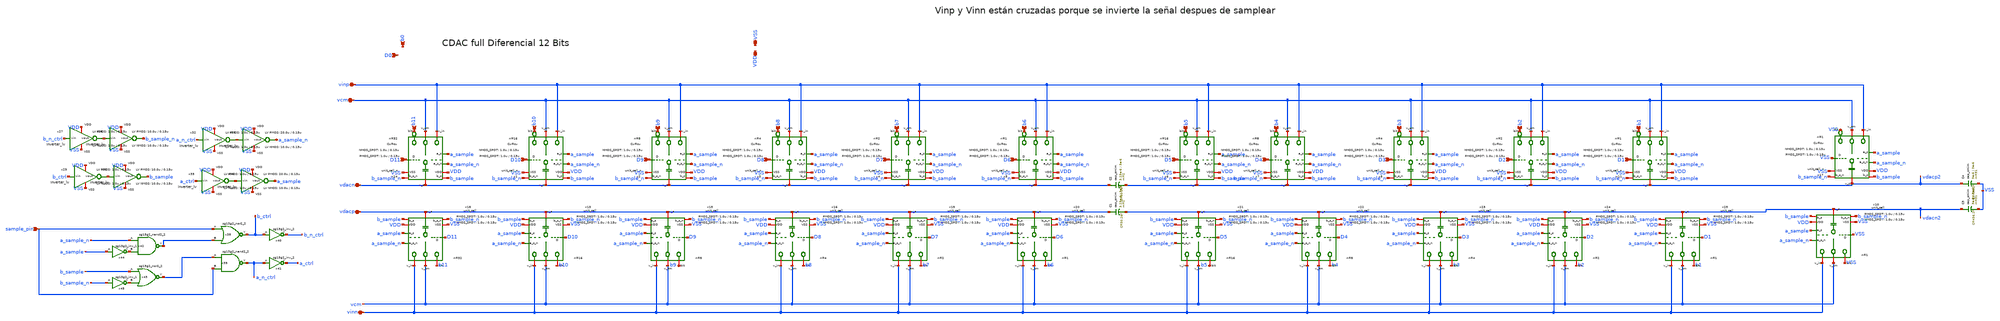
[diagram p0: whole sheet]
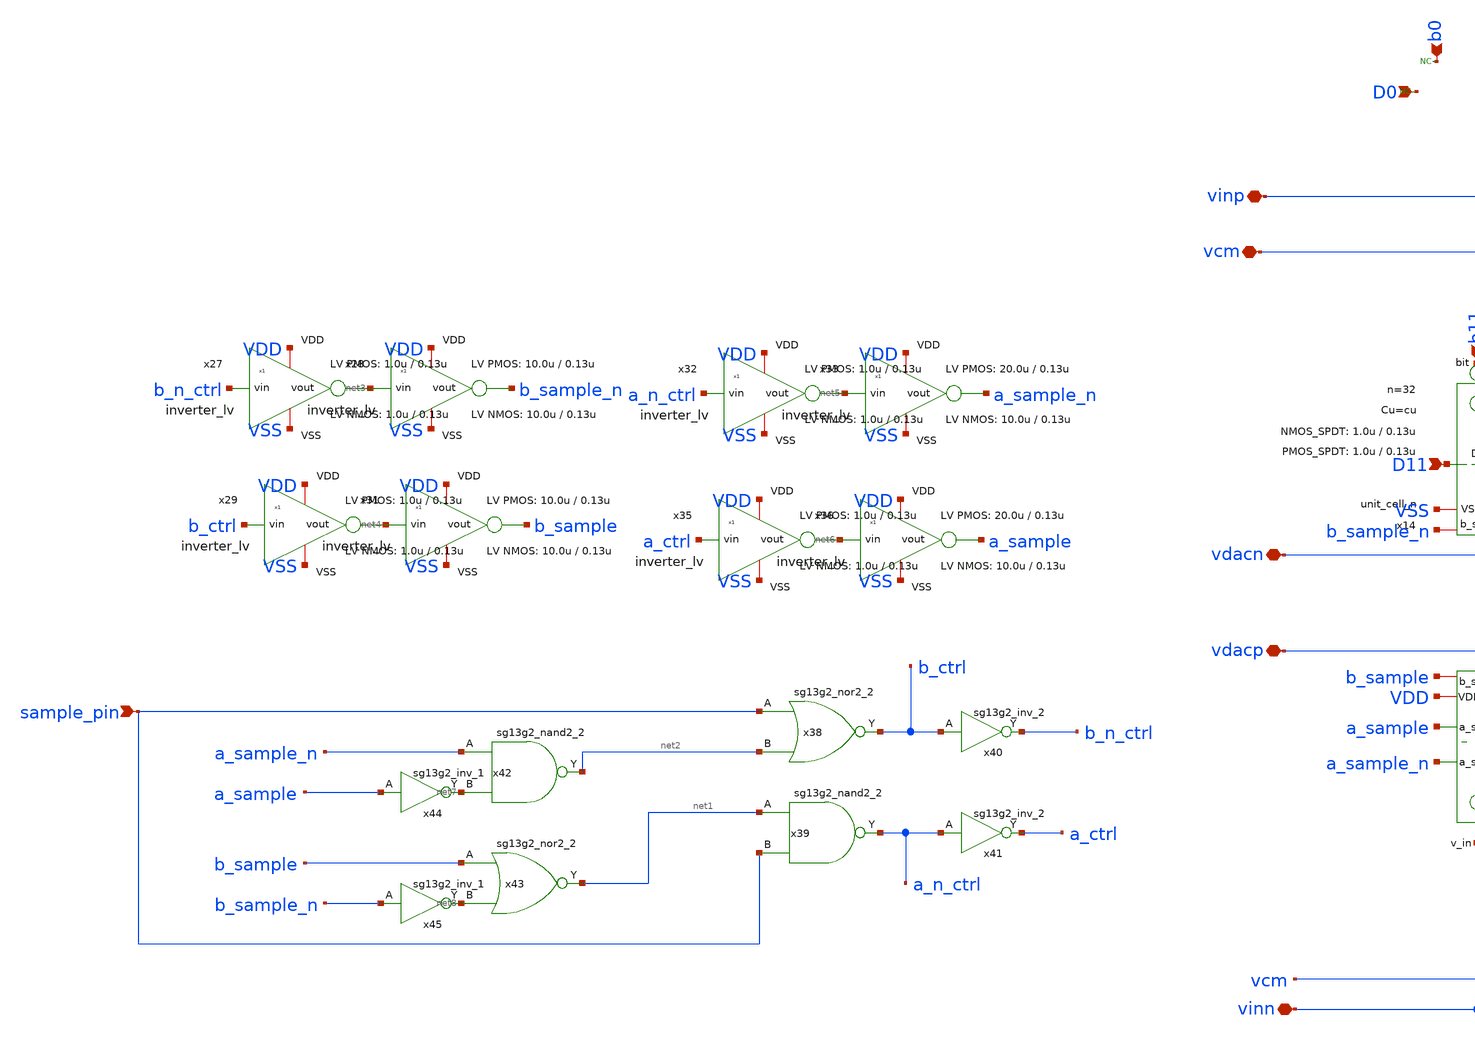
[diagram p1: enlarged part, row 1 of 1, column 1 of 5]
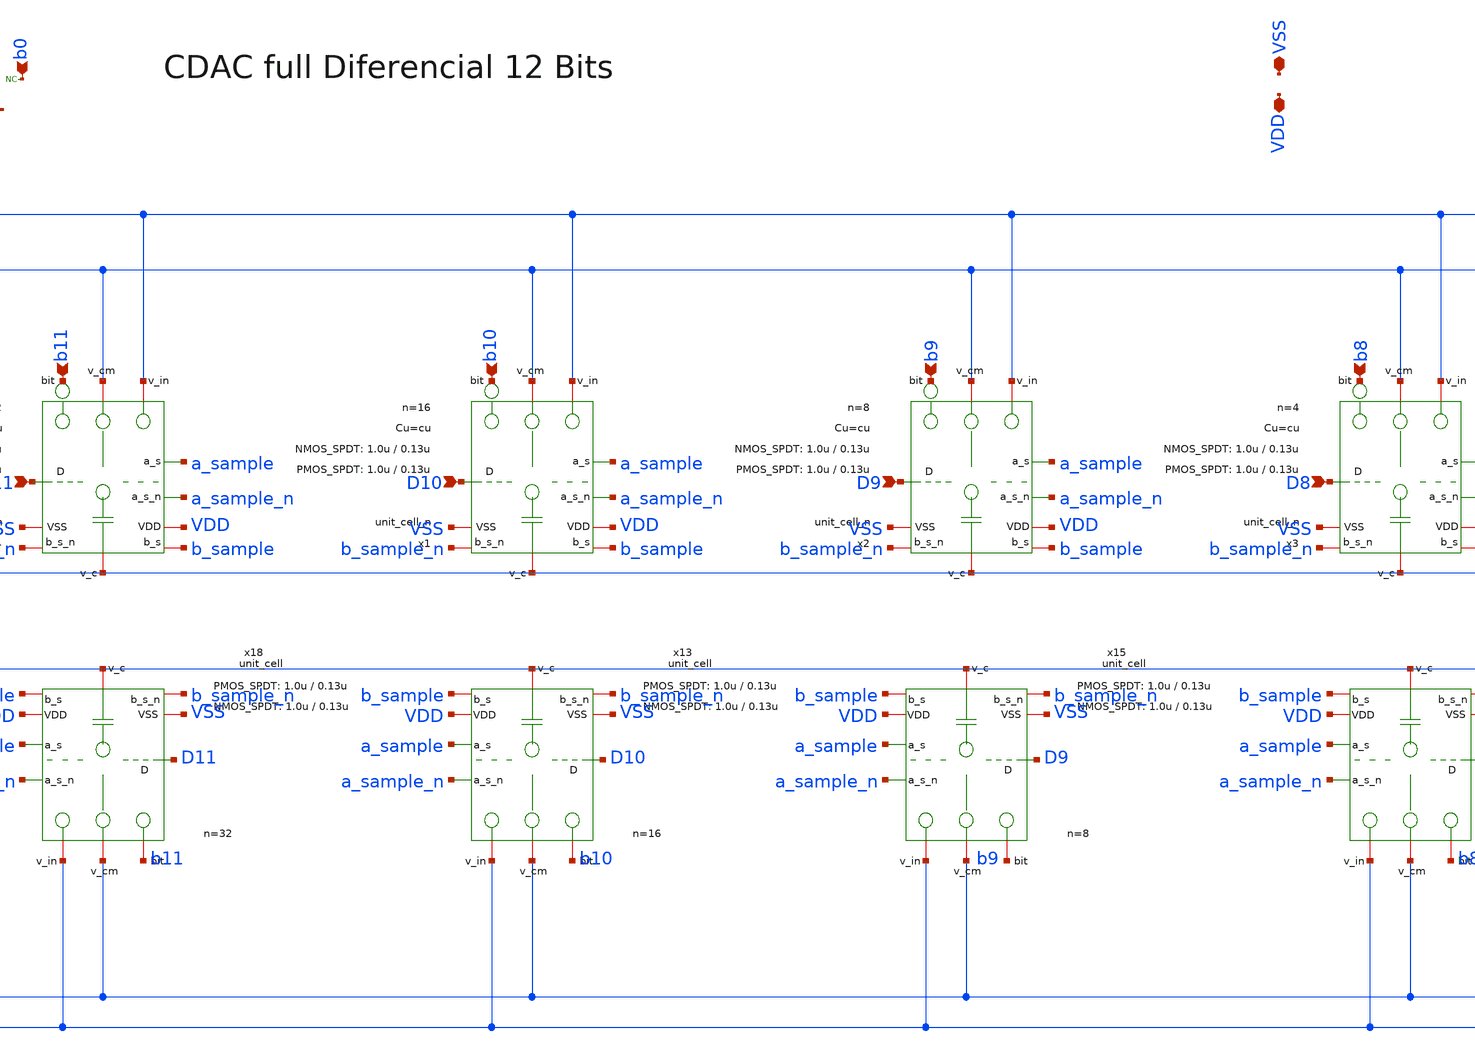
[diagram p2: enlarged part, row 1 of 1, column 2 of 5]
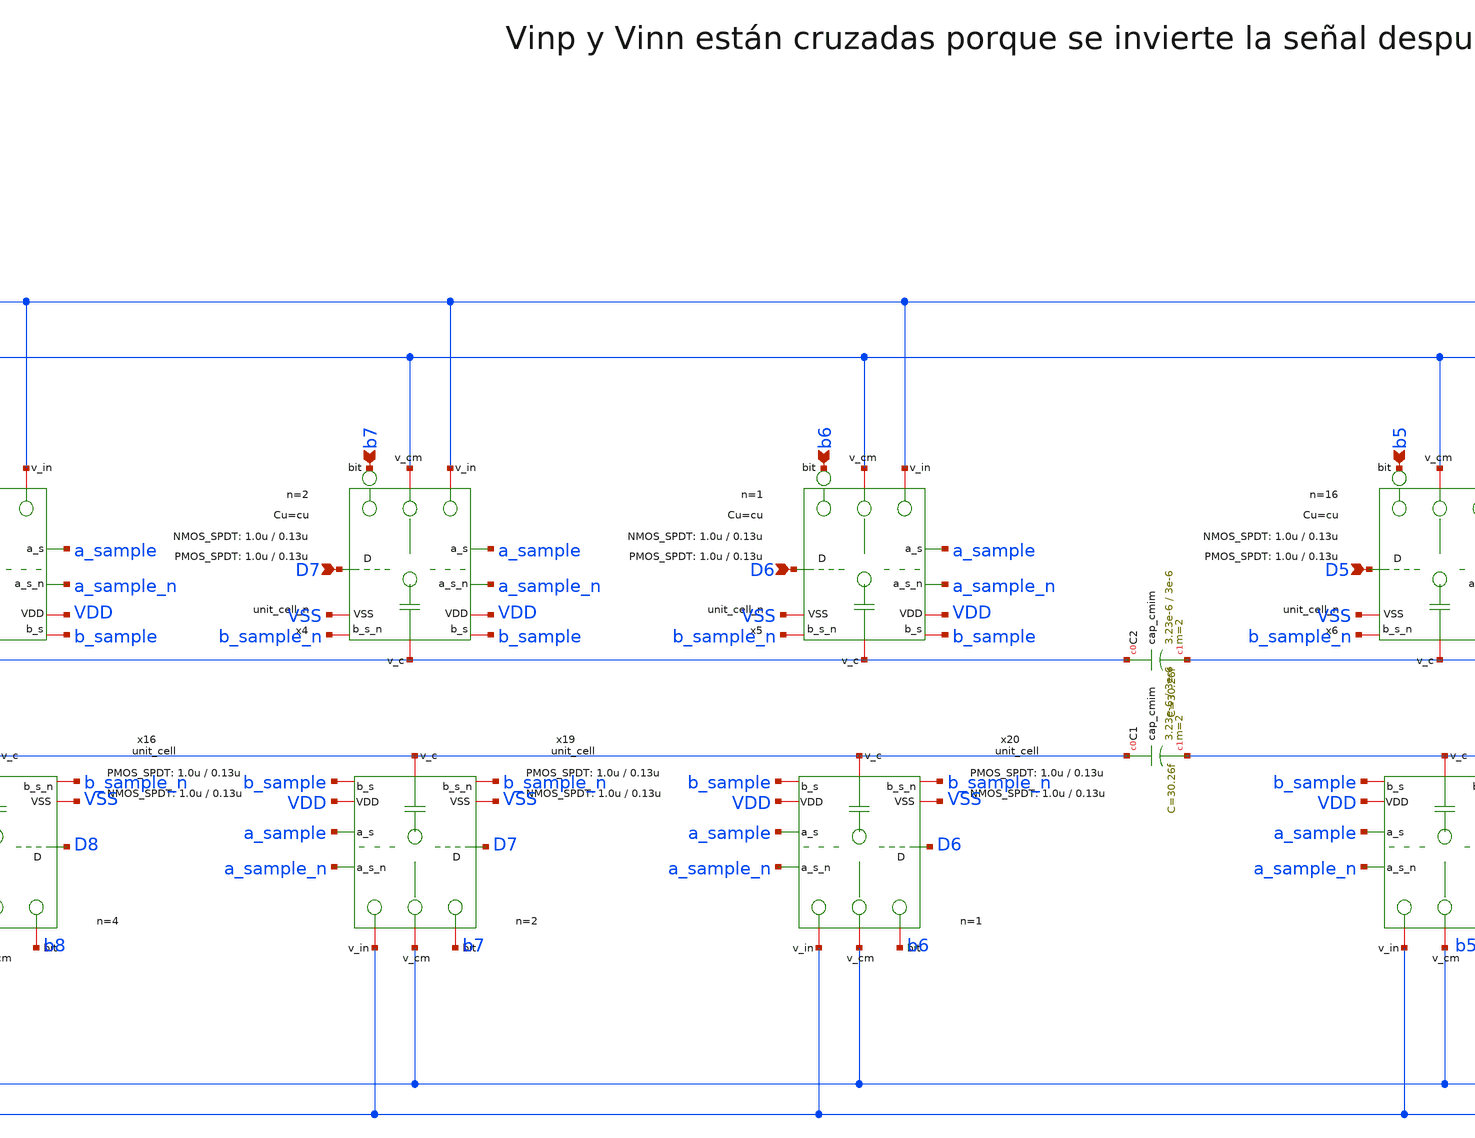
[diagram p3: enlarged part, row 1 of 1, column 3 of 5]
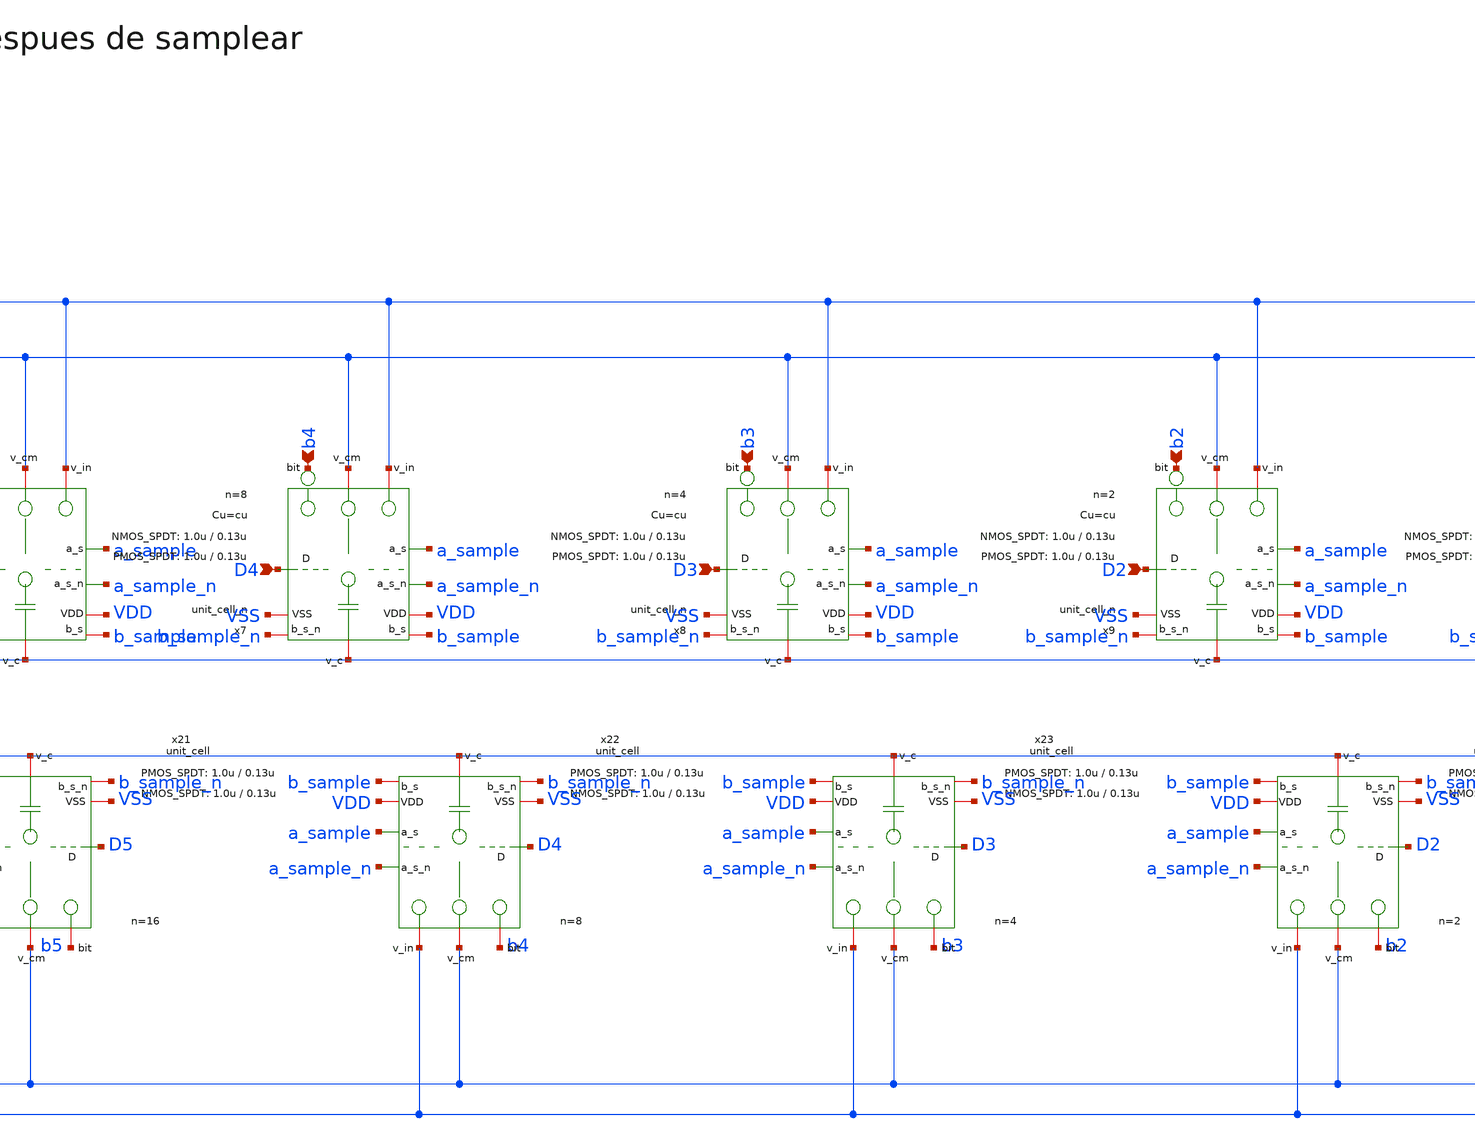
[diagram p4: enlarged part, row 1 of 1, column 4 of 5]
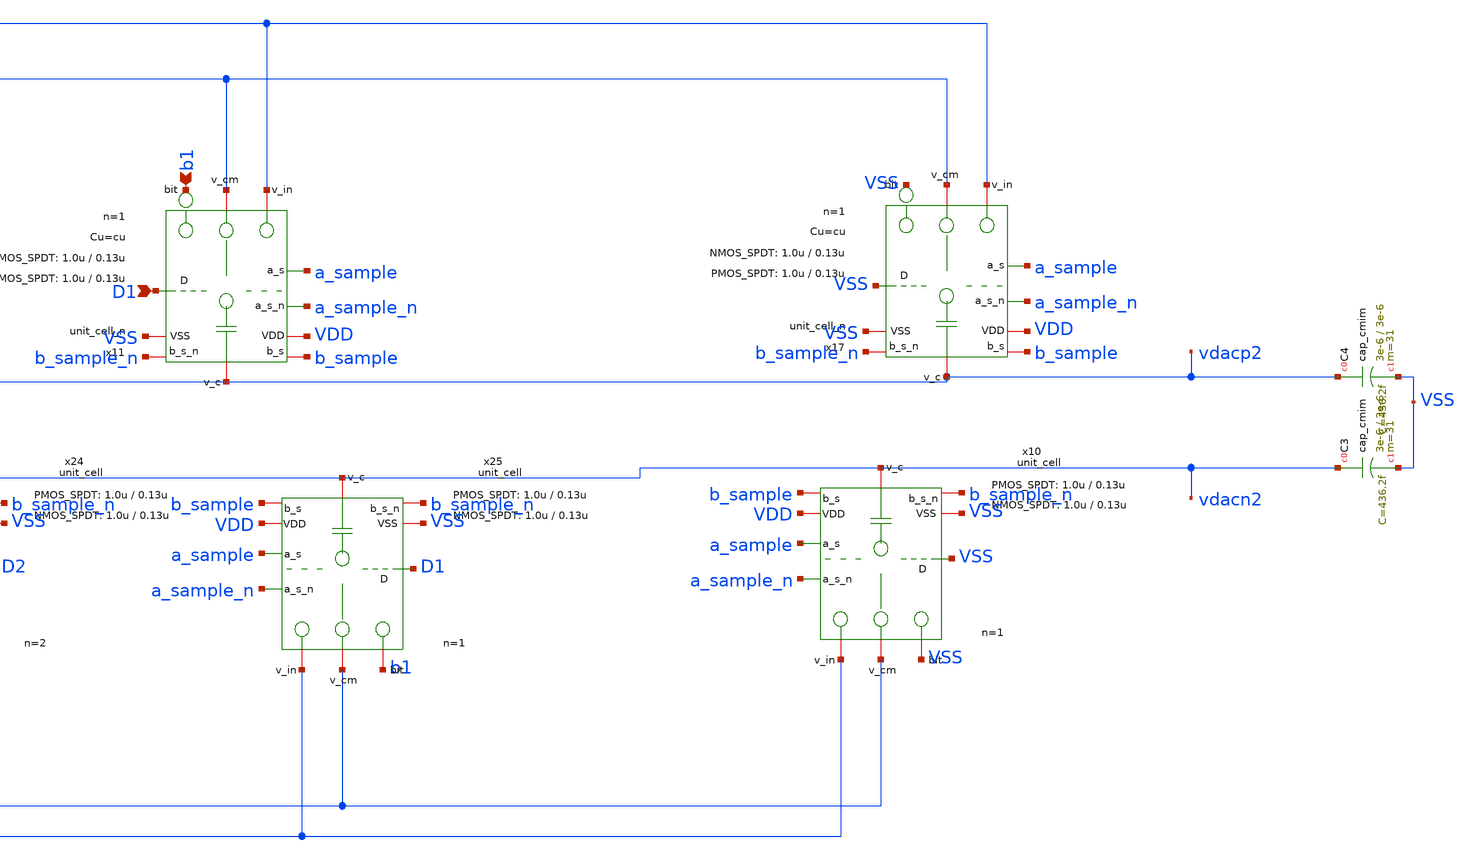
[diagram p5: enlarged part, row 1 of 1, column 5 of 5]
** sch_path: xschem/dac_icms_cell/dac.sch
* IHP-GmbH/IHP-Open-PDK/ihp-sg13g2/libs.tech/xschem/sg13g2_stdcells/sg13g2_inv_2.sch:
* Copyright 2023 IHP PDK Authors
* Licensed under the Apache License, Version 2.0 (the "License");
**.subckt dac D0 b0 vinn vcm sample_pin vinp vdacp vdacn VSS VDD D1 b1 D2 b2 D3 b3 D4 b4 D5 b5 b6 D7
*+ b7 D8 b8 D9 b9 D10 b10 D11 b11 D6
*.ipin D0
*.ipin b0
*.iopin vinn
*.iopin vcm
*.ipin sample_pin
*.iopin vinp
*.iopin vdacp
*.iopin vdacn
*.iopin VSS
*.iopin VDD
*.ipin D1
*.ipin b1
*.ipin D2
*.ipin b2
*.ipin D3
*.ipin b3
*.ipin D4
*.ipin b4
*.ipin D5
*.ipin b5
*.ipin b6
*.ipin D7
*.ipin b7
*.ipin D8
*.ipin b8
*.ipin D9
*.ipin b9
*.ipin D10
*.ipin b10
*.ipin D11
*.ipin b11
*.ipin D6
x14 VDD D11 VSS vdacn b11 vcm vinp a_sample a_sample_n b_sample b_sample_n unit_cell_n W_P=
+ L_P_SPDT=0.13u W_N= L_N_SPDT=0.13u Cu=cu n=32
x18 VDD D11 VSS vdacp b11 vcm vinn a_sample a_sample_n b_sample b_sample_n unit_cell W_P_SPDT=1.0u
+ L_P_SPDT=0.13u W_N_SPDT=1.0u L_N_SPDT=0.13u Cu=cu n=32
x1 VDD D10 VSS vdacn b10 vcm vinp a_sample a_sample_n b_sample b_sample_n unit_cell_n W_P=
+ L_P_SPDT=0.13u W_N= L_N_SPDT=0.13u Cu=cu n=16
x2 VDD D9 VSS vdacn b9 vcm vinp a_sample a_sample_n b_sample b_sample_n unit_cell_n W_P=
+ L_P_SPDT=0.13u W_N= L_N_SPDT=0.13u Cu=cu n=8
x3 VDD D8 VSS vdacn b8 vcm vinp a_sample a_sample_n b_sample b_sample_n unit_cell_n W_P=
+ L_P_SPDT=0.13u W_N= L_N_SPDT=0.13u Cu=cu n=4
x4 VDD D7 VSS vdacn b7 vcm vinp a_sample a_sample_n b_sample b_sample_n unit_cell_n W_P=1.0u
+ L_P_SPDT=0.13u W_N=1.0u L_N_SPDT=0.13u Cu=cu n=2
x5 VDD D6 VSS vdacn b6 vcm vinp a_sample a_sample_n b_sample b_sample_n unit_cell_n W_P=
+ L_P_SPDT=0.13u W_N= L_N_SPDT=0.13u Cu=cu n=1
x6 VDD D5 VSS vdacp2 b5 vcm vinp a_sample a_sample_n b_sample b_sample_n unit_cell_n W_P=
+ L_P_SPDT=0.13u W_N= L_N_SPDT=0.13u Cu=cu n=16
x7 VDD D4 VSS vdacp2 b4 vcm vinp a_sample a_sample_n b_sample b_sample_n unit_cell_n W_P=
+ L_P_SPDT=0.13u W_N= L_N_SPDT=0.13u Cu=cu n=8
x8 VDD D3 VSS vdacp2 b3 vcm vinp a_sample a_sample_n b_sample b_sample_n unit_cell_n W_P=
+ L_P_SPDT=0.13u W_N= L_N_SPDT=0.13u Cu=cu n=4
x9 VDD D2 VSS vdacp2 b2 vcm vinp a_sample a_sample_n b_sample b_sample_n unit_cell_n W_P=
+ L_P_SPDT=0.13u W_N= L_N_SPDT=0.13u Cu=cu n=2
x11 VDD D1 VSS vdacp2 b1 vcm vinp a_sample a_sample_n b_sample b_sample_n unit_cell_n W_P=
+ L_P_SPDT=0.13u W_N= L_N_SPDT=0.13u Cu=cu n=1
x13 VDD D10 VSS vdacp b10 vcm vinn a_sample a_sample_n b_sample b_sample_n unit_cell W_P_SPDT=1.0u
+ L_P_SPDT=0.13u W_N_SPDT=1.0u L_N_SPDT=0.13u Cu=cu n=16
x15 VDD D9 VSS vdacp b9 vcm vinn a_sample a_sample_n b_sample b_sample_n unit_cell W_P_SPDT=1.0u
+ L_P_SPDT=0.13u W_N_SPDT=1.0u L_N_SPDT=0.13u Cu=cu n=8
x16 VDD D8 VSS vdacp b8 vcm vinn a_sample a_sample_n b_sample b_sample_n unit_cell W_P_SPDT=1.0u
+ L_P_SPDT=0.13u W_N_SPDT=1.0u L_N_SPDT=0.13u Cu=cu n=4
x19 VDD D7 VSS vdacp b7 vcm vinn a_sample a_sample_n b_sample b_sample_n unit_cell W_P_SPDT=1.0u
+ L_P_SPDT=0.13u W_N_SPDT=1.0u L_N_SPDT=0.13u Cu=cu n=2
x20 VDD D6 VSS vdacp b6 vcm vinn a_sample a_sample_n b_sample b_sample_n unit_cell W_P_SPDT=1.0u
+ L_P_SPDT=0.13u W_N_SPDT=1.0u L_N_SPDT=0.13u Cu=cu n=1
x21 VDD D5 VSS vdacn2 b5 vcm vinn a_sample a_sample_n b_sample b_sample_n unit_cell W_P_SPDT=1.0u
+ L_P_SPDT=0.13u W_N_SPDT=1.0u L_N_SPDT=0.13u Cu=cu n=16
x22 VDD D4 VSS vdacn2 b4 vcm vinn a_sample a_sample_n b_sample b_sample_n unit_cell W_P_SPDT=1.0u
+ L_P_SPDT=0.13u W_N_SPDT=1.0u L_N_SPDT=0.13u Cu=cu n=8
x23 VDD D3 VSS vdacn2 b3 vcm vinn a_sample a_sample_n b_sample b_sample_n unit_cell W_P_SPDT=1.0u
+ L_P_SPDT=0.13u W_N_SPDT=1.0u L_N_SPDT=0.13u Cu=cu n=4
x24 VDD D2 VSS vdacn2 b2 vcm vinn a_sample a_sample_n b_sample b_sample_n unit_cell W_P_SPDT=1.0u
+ L_P_SPDT=0.13u W_N_SPDT=1.0u L_N_SPDT=0.13u Cu=cu n=2
x25 VDD D1 VSS vdacn2 b1 vcm vinn a_sample a_sample_n b_sample b_sample_n unit_cell W_P_SPDT=1.0u
+ L_P_SPDT=0.13u W_N_SPDT=1.0u L_N_SPDT=0.13u Cu=cu n=1
x27 VDD b_n_ctrl net3 VSS inverter_lv W_P=1.0u L_P=0.13u W_N=1.0u L_N=0.13u N_C=1
x28 VDD net3 b_sample_n VSS inverter_lv W_P=10.0u L_P=0.13u W_N=10.0u L_N=0.13u N_C=1
x29 VDD b_ctrl net4 VSS inverter_lv W_P=1.0u L_P=0.13u W_N=1.0u L_N=0.13u N_C=1
x31 VDD net4 b_sample VSS inverter_lv W_P=10.0u L_P=0.13u W_N=10.0u L_N=0.13u N_C=1
x32 VDD a_n_ctrl net5 VSS inverter_lv W_P=1.0u L_P=0.13u W_N=1.0u L_N=0.13u N_C=1
x33 VDD net5 a_sample_n VSS inverter_lv W_P=20.0u L_P=0.13u W_N=10.0u L_N=0.13u N_C=1
x35 VDD a_ctrl net6 VSS inverter_lv W_P=1.0u L_P=0.13u W_N=1.0u L_N=0.13u N_C=1
x36 VDD net6 a_sample VSS inverter_lv W_P=20.0u L_P=0.13u W_N=10.0u L_N=0.13u N_C=1
x38 b_ctrl sample_pin net2 VDD VSS sg13g2_nor2_2
x39 a_n_ctrl net1 sample_pin VDD VSS sg13g2_nand2_2
x40 b_n_ctrl b_ctrl VDD VSS sg13g2_inv_2
x41 a_ctrl a_n_ctrl VDD VSS sg13g2_inv_2
x42 net2 a_sample_n net7 VDD VSS sg13g2_nand2_2
x43 net1 b_sample net8 VDD VSS sg13g2_nor2_2
x44 net7 a_sample VDD VSS sg13g2_inv_1
x45 net8 b_sample_n VDD VSS sg13g2_inv_1
XC1 vdacp vdacn2 cap_cmim w=3.23e-6 l=3e-6 m=2 mm_ok=1
XC2 vdacn vdacp2 cap_cmim w=3.23e-6 l=3e-6 m=2 mm_ok=1
x10 VDD VSS VSS vdacn2 VSS vcm vinn a_sample a_sample_n b_sample b_sample_n unit_cell W_P_SPDT=1.0u
+ L_P_SPDT=0.13u W_N_SPDT=1.0u L_N_SPDT=0.13u Cu=cu n=1
x17 VDD VSS VSS vdacp2 VSS vcm vinp a_sample a_sample_n b_sample b_sample_n unit_cell_n W_P=
+ L_P_SPDT=0.13u W_N= L_N_SPDT=0.13u Cu=cu n=1
XC3 vdacn2 VSS cap_cmim w=3e-6 l=3e-6 m=31 mm_ok=1
XC4 vdacp2 VSS cap_cmim w=3e-6 l=3e-6 m=31 mm_ok=1
* noconn b0
* noconn D0
**.ends

* expanding   symbol:  dac_icms_cell/unit_cell_n.sym # of pins=11
** sym_path: xschem/dac_icms_cell/unit_cell_n.sym
** sch_path: xschem/dac_icms_cell/unit_cell_n.sch
.subckt unit_cell_n VDD d VSS v_top bit v_cm v_in a_sample a_sample_n b_sample b_sample_n
+  W_P_SPDT=1.0u L_P_SPDT=0.13u W_N_SPDT=1.0u L_N_SPDT=0.13u Cu=8f n=1
*.iopin VSS
*.iopin v_in
*.iopin VDD
*.ipin d
*.ipin bit
*.iopin v_top
*.iopin v_cm
*.ipin a_sample
*.ipin a_sample_n
*.ipin b_sample
*.ipin b_sample_n
x1 VDD d VSS net1 bit v_cm v_in b_sample_n b_sample dac_switch_n W_P_TG=3.0u L_P_TG=0.13u
+ W_N_TG=1.0u L_N_TG=0.13u n=n
C1 net1 v_top Cu m=n
x2 VDD a_sample VSS v_cm v_top a_sample_n transmission_gate_lv_w_dummy W_P=W_P_SPDT L_P=L_P_SPDT
+ W_N=W_N_SPDT L_N=L_N_SPDT W_P_D=1.0u L_P_D=0.13u W_N_D=1.0u L_N_D=0.13u n=n
.ends


* expanding   symbol:  dac_icms_cell/unit_cell.sym # of pins=11
** sym_path: xschem/dac_icms_cell/unit_cell.sym
** sch_path: xschem/dac_icms_cell/unit_cell.sch
.subckt unit_cell VDD d VSS v_top bit v_cm v_in a_sample a_sample_n b_sample b_sample_n
+  W_P_SPDT=1.0u L_P_SPDT=0.13u W_N_SPDT=1.0u L_N_SPDT=0.13u Cu=8f n=1
*.iopin VSS
*.iopin v_in
*.ipin d
*.ipin bit
*.iopin v_top
*.iopin v_cm
*.ipin b_sample
*.ipin b_sample_n
*.ipin a_sample
*.ipin a_sample_n
*.iopin VDD
S7 net2 net3 d VSS SW1
C1 net1 v_top Cu m=n
S9 net3 net1 b_sample b_sample_n SW1
S10 v_in net1 b_sample_n b_sample SW1
S11 v_top v_cm a_sample a_sample_n SW1
S12 VSS net2 bit VSS SW1
S13 net2 VDD bitn VSS SW1
S14 net3 v_cm dn VSS SW1
x8 VDD bit bitn VSS inverter_lv W_P=W_P_SPDT L_P=L_P_SPDT W_N=W_N_SPDT L_N=L_N_SPDT N_C=1
x1 VDD d dn VSS inverter_lv W_P=W_P_SPDT L_P=L_P_SPDT W_N=W_N_SPDT L_N=L_N_SPDT N_C=1
.ends


* expanding   symbol:  inverter/inverter_lv.sym # of pins=4
** sym_path: xschem/inverter/inverter_lv.sym
** sch_path: xschem/inverter/inverter_lv.sch
.subckt inverter_lv VDD vin vout VSS  W_P=3.0u L_P=0.13u W_N=1.0u L_N=0.13u N_C=1
*.ipin vin
*.iopin VDD
*.iopin VSS
*.opin vout
XM1 vout vin VDD VDD sg13_lv_pmos w=W_P l=L_P ng=1 m={N_C} mm_ok=1
XM2 vout vin VSS VSS sg13_lv_nmos w=W_N l=L_N ng=1 m={N_C} mm_ok=1
.ends


* expanding   symbol:  sg13g2_stdcells/sg13g2_nor2_2.sym # of pins=3
** sym_path: sg13g2_stdcells/sg13g2_nor2_2.sym
** sch_path: sg13g2_stdcells/sg13g2_nor2_2.sch
.subckt sg13g2_nor2_2 Y A B VDD VSS
*.opin Y
*.ipin B
*.ipin A
*.iopin VDD
*.iopin VSS
XM1 Y A VSS VSS sg13_lv_nmos w=1.48u l=130.00n ng=2 m=1 mm_ok=1
XM2 Y B VSS VSS sg13_lv_nmos w=1.48u l=130.00n ng=2 m=1 mm_ok=1
XM3 net1 A VDD VDD sg13_lv_pmos w=2.24u l=130.00n ng=2 m=1 mm_ok=1
XM4 Y B net1 VDD sg13_lv_pmos w=2.24u l=130.00n ng=2 m=1 mm_ok=1
.ends


* expanding   symbol:  sg13g2_stdcells/sg13g2_nand2_2.sym # of pins=3
** sym_path: sg13g2_stdcells/sg13g2_nand2_2.sym
** sch_path: sg13g2_stdcells/sg13g2_nand2_2.sch
.subckt sg13g2_nand2_2 Y A B VDD VSS
*.iopin VDD
*.iopin VSS
*.opin Y
*.ipin B
*.ipin A
XM1 Y A net1 VSS sg13_lv_nmos w=1.44u l=130.00n ng=2 m=1 mm_ok=1
XM2 net1 B VSS VSS sg13_lv_nmos w=1.44u l=130.00n ng=2 m=1 mm_ok=1
XM3 Y A VDD VDD sg13_lv_pmos w=2.24u l=130.00n ng=2 m=1 mm_ok=1
XM4 Y B VDD VDD sg13_lv_pmos w=2.24u l=130.00n ng=2 m=1 mm_ok=1
.ends


* expanding   symbol:  sg13g2_stdcells/sg13g2_inv_2.sym # of pins=2
** sym_path: sg13g2_stdcells/sg13g2_inv_2.sym
** sch_path: sg13g2_stdcells/sg13g2_inv_2.sch
.subckt sg13g2_inv_2 Y A VDD VSS
*.opin Y
*.ipin A
*.iopin VDD
*.iopin VSS
XM1 Y A VSS VSS sg13_lv_nmos w=1.48u l=130.00n ng=2 m=1 mm_ok=1
XM2 Y A VDD VDD sg13_lv_pmos w=2.24u l=130.00n ng=2 m=1 mm_ok=1
.ends


* expanding   symbol:  sg13g2_stdcells/sg13g2_inv_1.sym # of pins=2
** sym_path: sg13g2_stdcells/sg13g2_inv_1.sym
** sch_path: sg13g2_stdcells/sg13g2_inv_1.sch
.subckt sg13g2_inv_1 Y A VDD VSS
*.opin Y
*.ipin A
*.iopin VDD
*.iopin VSS
XM1 Y A VSS VSS sg13_lv_nmos w=740.00n l=130.00n ng=1 m=1 mm_ok=1
XM2 Y A VDD VDD sg13_lv_pmos w=1.12u l=130.00n ng=1 m=1 mm_ok=1
.ends


* expanding   symbol:  dac_icms_cell/dac_switch_n.sym # of pins=9
** sym_path: xschem/dac_icms_cell/dac_switch_n.sym
** sch_path: xschem/dac_icms_cell/dac_switch_n.sch
.subckt dac_switch_n VDD d VSS v_cap bit v_cm v_in sample sample_n  W_P_TG=3.0u L_P_TG=0.13u
+ W_N_TG=1.0u L_N_TG=0.13u n=1
*.iopin v_in
*.iopin v_cap
*.iopin VDD
*.iopin VSS
*.ipin d
*.iopin v_cm
*.ipin bit
*.ipin sample
*.ipin sample_n
x8 VDD d d_n VSS inverter_lv W_P=W_P_TG L_P=L_P_TG W_N=W_N_TG L_N=L_N_TG N_C=1
XM1 v_cap net3 VSS VSS sg13_lv_nmos w=1u l=0.2u ng=1 m=n mm_ok=1
XM3 v_cap net4 VDD VDD sg13_lv_pmos w=1.2u l=0.13u ng=1 m=n mm_ok=1
x2 VDD net2 VSS v_cap v_cm net1 transmission_gate_lv_w_dummy W_P=W_P_TG L_P=L_P_TG W_N=W_N_TG
+ L_N=L_N_TG W_P_D=1.0u L_P_D=0.13u W_N_D=1.0u L_N_D=0.13u n=n
x1 VDD sample VSS v_cap v_in sample_n transmission_gate_lv_w_dummy W_P=W_P_TG L_P=L_P_TG W_N=W_N_TG
+ L_N=L_N_TG W_P_D=1.0u L_P_D=0.13u W_N_D=1.0u L_N_D=0.13u n=n
x23 net5 bit d VDD VSS sg13g2_nand2_1
x46 net6 net9 d VDD VSS sg13g2_and2_1
x4 VDD net5 net4 VSS buffer_lv W_P_INV=3.0u L_P_INV=0.13u W_N_INV=1.0u L_N_INV=0.13u
x5 VDD net6 net3 VSS buffer_lv W_P_INV=3.0u L_P_INV=0.13u W_N_INV=1.0u L_N_INV=0.13u
x3 net7 d sample VDD VSS sg13g2_nor2_1
x6 net8 d sample VDD VSS sg13g2_or2_1
x7 VDD net7 net2 VSS buffer_lv W_P_INV=3.0u L_P_INV=0.13u W_N_INV=1.0u L_N_INV=0.13u
x9 VDD net8 net1 VSS buffer_lv W_P_INV=3.0u L_P_INV=0.13u W_N_INV=1.0u L_N_INV=0.13u
x32 net9 bit VDD VSS sg13g2_inv_1
.ends


* expanding   symbol:  transmission_gate/transmission_gate_lv_w_dummy.sym # of pins=6
** sym_path: xschem/transmission_gate/transmission_gate_lv_w_dummy.sym
** sch_path: xschem/transmission_gate/transmission_gate_lv_w_dummy.sch
.subckt transmission_gate_lv_w_dummy VDD di_tg_ctrl VSS v_b v_a di_tg_ctrl_n  W_P=2.0u L_P=0.13u
+ W_N=2.0u L_N=0.13u W_P_D=1.0u L_P_D=0.13u W_N_D=1.0u L_N_D=0.13u n=1
*.iopin v_a
*.iopin v_b
*.iopin VDD
*.iopin VSS
*.ipin di_tg_ctrl
*.ipin di_tg_ctrl_n
XM1 v_a di_tg_ctrl v_b VSS sg13_lv_nmos w=W_N l=L_N ng=1 m=n mm_ok=1
XM2 v_a di_tg_ctrl_n v_b VDD sg13_lv_pmos w=W_P l=L_P ng=1 m=n mm_ok=1
XMdummy2 v_b di_tg_ctrl v_b VDD sg13_lv_pmos w=W_P l=L_P ng=1 m={n/2} mm_ok=1
XMdummy1 v_b di_tg_ctrl_n v_b VSS sg13_lv_nmos w=W_N l=L_N ng=1 m={n/2} mm_ok=1
.ends


* expanding   symbol:  sg13g2_stdcells/sg13g2_nand2_1.sym # of pins=3
** sym_path: sg13g2_stdcells/sg13g2_nand2_1.sym
** sch_path: sg13g2_stdcells/sg13g2_nand2_1.sch
.subckt sg13g2_nand2_1 Y A B VDD VSS
*.iopin VDD
*.iopin VSS
*.ipin A
*.ipin B
*.opin Y
XM1 Y A net1 VSS sg13_lv_nmos w=740.00n l=130.00n ng=1 m=1 mm_ok=1
XM2 net1 B VSS VSS sg13_lv_nmos w=740.00n l=130.00n ng=1 m=1 mm_ok=1
XM3 Y A VDD VDD sg13_lv_pmos w=1.12u l=130.00n ng=1 m=1 mm_ok=1
XM4 Y B VDD VDD sg13_lv_pmos w=1.12u l=130.00n ng=1 m=1 mm_ok=1
.ends


* expanding   symbol:  sg13g2_stdcells/sg13g2_and2_1.sym # of pins=3
** sym_path: sg13g2_stdcells/sg13g2_and2_1.sym
** sch_path: sg13g2_stdcells/sg13g2_and2_1.sch
.subckt sg13g2_and2_1 X A B VDD VSS
*.ipin A
*.ipin B
*.opin X
*.iopin VDD
*.iopin VSS
XM1 net1 A net2 VSS sg13_lv_nmos w=640.00n l=130.00n ng=1 m=1 mm_ok=1
XM2 net2 B VSS VSS sg13_lv_nmos w=640.00n l=130.00n ng=1 m=1 mm_ok=1
XM3 X net1 VSS VSS sg13_lv_nmos w=740.00n l=130.00n ng=1 m=1 mm_ok=1
XM4 net1 B VDD VDD sg13_lv_pmos w=840.00n l=130.00n ng=1 m=1 mm_ok=1
XM5 net1 A VDD VDD sg13_lv_pmos w=840.00n l=130.00n ng=1 m=1 mm_ok=1
XM6 X net1 VDD VDD sg13_lv_pmos w=1.12u l=130.00n ng=1 m=1 mm_ok=1
.ends


* expanding   symbol:  buffer/buffer_lv.sym # of pins=4
** sym_path: buffer/buffer_lv.sym
** sch_path: buffer/buffer_lv.sch
.subckt buffer_lv VDD vin vout VSS  W_P_INV=3.0u L_P_INV=0.13u W_N_INV=1.0u L_N_INV=0.13u
*.ipin vin
*.iopin VDD
*.iopin VSS
*.opin vout
x1 VDD vin net1 VSS inverter_lv W_P=W_P_INV L_P=L_P_INV W_N=W_N_INV L_N=L_N_INV N_C=1
x2 VDD net1 vout VSS inverter_lv W_P=W_P_INV L_P=L_P_INV W_N=W_N_INV L_N=L_N_INV N_C=1
.ends


* expanding   symbol:  sg13g2_stdcells/sg13g2_nor2_1.sym # of pins=3
** sym_path: sg13g2_stdcells/sg13g2_nor2_1.sym
** sch_path: sg13g2_stdcells/sg13g2_nor2_1.sch
.subckt sg13g2_nor2_1 Y A B VDD VSS
*.opin Y
*.ipin B
*.ipin A
*.iopin VDD
*.iopin VSS
XM1 Y A VSS VSS sg13_lv_nmos w=740.00n l=130.00n ng=1 m=1 mm_ok=1
XM2 Y B VSS VSS sg13_lv_nmos w=740.00n l=130.00n ng=1 m=1 mm_ok=1
XM3 net1 A VDD VDD sg13_lv_pmos w=1.12u l=130.00n ng=1 m=1 mm_ok=1
XM4 Y B net1 VDD sg13_lv_pmos w=1.12u l=130.00n ng=1 m=1 mm_ok=1
.ends


* expanding   symbol:  sg13g2_stdcells/sg13g2_or2_1.sym # of pins=3
** sym_path: sg13g2_stdcells/sg13g2_or2_1.sym
** sch_path: sg13g2_stdcells/sg13g2_or2_1.sch
.subckt sg13g2_or2_1 X A B VDD VSS
*.opin X
*.ipin B
*.ipin A
*.iopin VDD
*.iopin VSS
XM1 net1 B VSS VSS sg13_lv_nmos w=550.00n l=130.00n ng=1 m=1 mm_ok=1
XM2 net1 A VSS VSS sg13_lv_nmos w=550.00n l=130.00n ng=1 m=1 mm_ok=1
XM3 X net1 VSS VSS sg13_lv_nmos w=740.00n l=130.00n ng=1 m=1 mm_ok=1
XM4 net2 A VDD VDD sg13_lv_pmos w=840.00n l=130.00n ng=1 m=1 mm_ok=1
XM5 net1 B net2 VDD sg13_lv_pmos w=840.00n l=130.00n ng=1 m=1 mm_ok=1
XM6 X net1 VDD VDD sg13_lv_pmos w=1.12u l=130.00n ng=1 m=1 mm_ok=1
.ends

**** begin user architecture code
.MODEL SW1 SW   VT=0.9 VH=0.01  RON={ro/2} ROFF=10G
**** end user architecture code
.end
